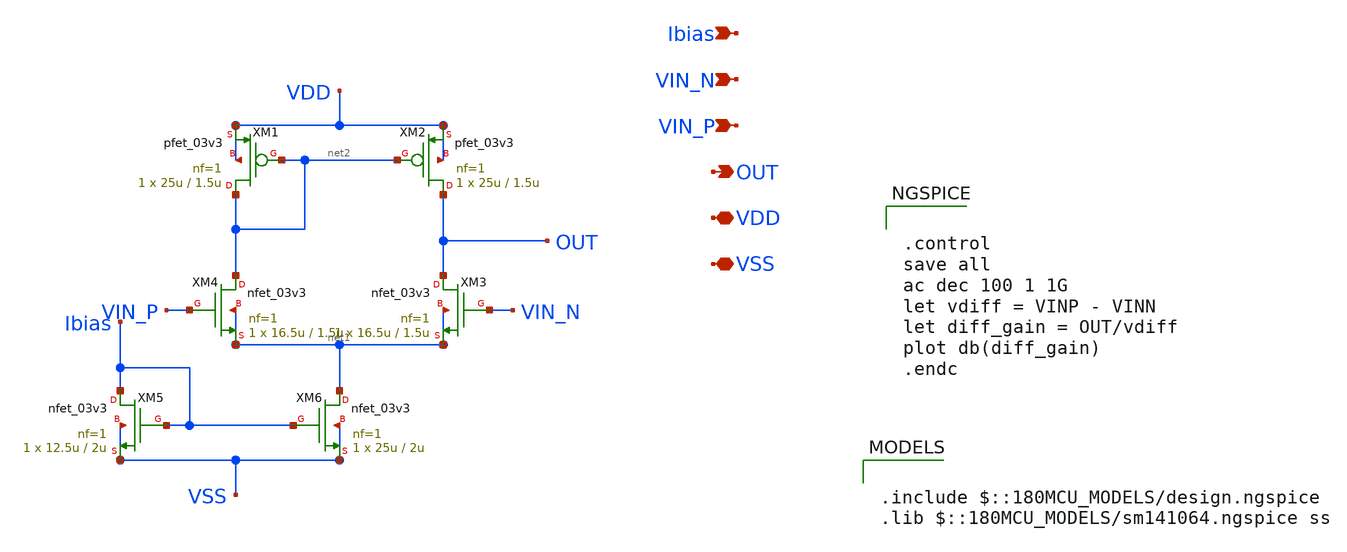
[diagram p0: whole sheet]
** sch_path: week02_current_diffpair/tugas5_cascode_current_mirror/n-5t-ota.sch
**.subckt n-5t-ota VIN_N VIN_P OUT VDD VSS Ibias
*.ipin VIN_N
*.ipin VIN_P
*.opin OUT
*.iopin VDD
*.iopin VSS
*.ipin Ibias
XM1 net2 net2 VDD VDD pfet_03v3 L=1.5u W=25u nf=1 ad='int((nf+1)/2) * W/nf * 0.18u' as='int((nf+2)/2) * W/nf * 0.18u'
+ pd='2*int((nf+1)/2) * (W/nf + 0.18u)' ps='2*int((nf+2)/2) * (W/nf + 0.18u)' nrd='0.18u / W' nrs='0.18u / W'
+ sa=0 sb=0 sd=0 m=1
XM2 OUT net2 VDD VDD pfet_03v3 L=1.5u W=25u nf=1 ad='int((nf+1)/2) * W/nf * 0.18u' as='int((nf+2)/2) * W/nf * 0.18u'
+ pd='2*int((nf+1)/2) * (W/nf + 0.18u)' ps='2*int((nf+2)/2) * (W/nf + 0.18u)' nrd='0.18u / W' nrs='0.18u / W'
+ sa=0 sb=0 sd=0 m=1
XM3 OUT VIN_N net1 net1 nfet_03v3 L=1.5u W=16.5u nf=1 ad='int((nf+1)/2) * W/nf * 0.18u' as='int((nf+2)/2) * W/nf * 0.18u'
+ pd='2*int((nf+1)/2) * (W/nf + 0.18u)' ps='2*int((nf+2)/2) * (W/nf + 0.18u)' nrd='0.18u / W' nrs='0.18u / W'
+ sa=0 sb=0 sd=0 m=1
XM4 net2 VIN_P net1 net1 nfet_03v3 L=1.5u W=16.5u nf=1 ad='int((nf+1)/2) * W/nf * 0.18u' as='int((nf+2)/2) * W/nf * 0.18u'
+ pd='2*int((nf+1)/2) * (W/nf + 0.18u)' ps='2*int((nf+2)/2) * (W/nf + 0.18u)' nrd='0.18u / W' nrs='0.18u / W'
+ sa=0 sb=0 sd=0 m=1
XM5 Ibias Ibias VSS VSS nfet_03v3 L=2u W=12.5u nf=1 ad='int((nf+1)/2) * W/nf * 0.18u' as='int((nf+2)/2) * W/nf * 0.18u'
+ pd='2*int((nf+1)/2) * (W/nf + 0.18u)' ps='2*int((nf+2)/2) * (W/nf + 0.18u)' nrd='0.18u / W' nrs='0.18u / W'
+ sa=0 sb=0 sd=0 m=1
XM6 net1 Ibias VSS VSS nfet_03v3 L=2u W=25u nf=1 ad='int((nf+1)/2) * W/nf * 0.18u' as='int((nf+2)/2) * W/nf * 0.18u'
+ pd='2*int((nf+1)/2) * (W/nf + 0.18u)' ps='2*int((nf+2)/2) * (W/nf + 0.18u)' nrd='0.18u / W' nrs='0.18u / W'
+ sa=0 sb=0 sd=0 m=1
**** begin user architecture code

.include $::180MCU_MODELS/design.ngspice
.lib $::180MCU_MODELS/sm141064.ngspice ss



.control
save all
ac dec 100 1 1G
let vdiff = VINP - VINN
let diff_gain = OUT/vdiff
plot db(diff_gain)
.endc


**** end user architecture code
**.ends
.end
